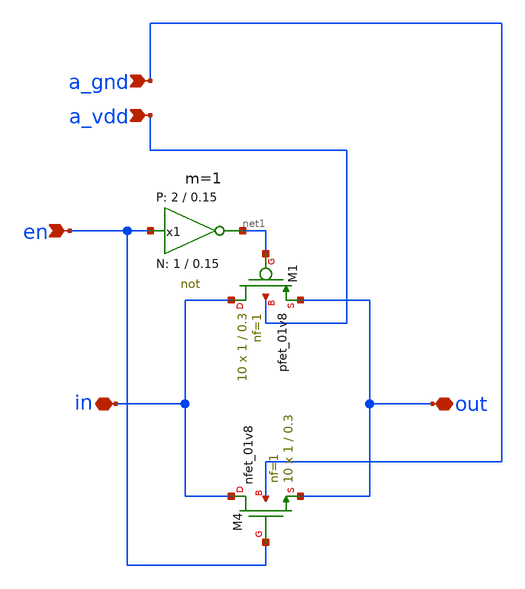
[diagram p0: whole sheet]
** sch_path: Schematics/ADC/sw/sw.sch
* StefanSchippers/xschem_sky130/sky130_tests/not.sch:
* Copyright 2021 Stefan Frederik Schippers
* Licensed under the Apache License, Version 2.0 (the "License");
**.subckt sw out in en a_gnd a_vdd
*.iopin out
*.iopin in
*.ipin en
*.ipin a_gnd
*.ipin a_vdd
XM4 in en out a_gnd sky130_fd_pr__nfet_01v8 L=0.3 W=1 nf=1 ad='int((nf+1)/2) * W/nf * 0.29' as='int((nf+2)/2) * W/nf * 0.29'
+ pd='2*int((nf+1)/2) * (W/nf + 0.29)' ps='2*int((nf+2)/2) * (W/nf + 0.29)' nrd='0.29 / W' nrs='0.29 / W'
+ sa=0 sb=0 sd=0 mult=10 m=10
XM1 in net1 out a_vdd sky130_fd_pr__pfet_01v8 L=0.3 W=1 nf=1 ad='int((nf+1)/2) * W/nf * 0.29' as='int((nf+2)/2) * W/nf * 0.29'
+ pd='2*int((nf+1)/2) * (W/nf + 0.29)' ps='2*int((nf+2)/2) * (W/nf + 0.29)' nrd='0.29 / W' nrs='0.29 / W'
+ sa=0 sb=0 sd=0 mult=10 m=10
x1 net1 en a_vdd a_gnd not W_N=1 L_N=0.15 W_P=2 L_P=0.15 m=1
**.ends

* expanding   symbol:  /home/richmond/pdk/sky130A/libs.tech/xschem/sky130_tests/not.sym # of pins=2
** sym_path: /home/richmond/pdk/sky130A/libs.tech/xschem/sky130_tests/not.sym
** sch_path: /home/richmond/pdk/sky130A/libs.tech/xschem/sky130_tests/not.sch
.subckt not y a VCCPIN VSSPIN     W_N=1 L_N=0.15 W_P=2 L_P=0.15
*.opin y
*.ipin a
XM1 DN a VSSPIN VSSPIN sky130_fd_pr__nfet_01v8 L=L_N W=W_N nf=1 ad='int((1 + 1)/2) * W_N / 1 * 0.29'
+ as='int((1 + 2)/2) * W_N / 1 * 0.29' pd='2*int((1 + 1)/2) * (W_N / 1 + 0.29)' ps='2*int((1 + 2)/2) * (W_N / 1 + 0.29)'
+ nrd='0.29 / W_N ' nrs='0.29 / W_N ' sa=0 sb=0 sd=0 mult=1 m=1
XM2 DP a VCCPIN VCCPIN sky130_fd_pr__pfet_01v8 L=L_P W=W_P nf=1 ad='int((nf+1)/2) * W/nf * 0.29' as='int((nf+2)/2) * W/nf * 0.29'
+ pd='2*int((nf+1)/2) * (W/nf + 0.29)' ps='2*int((nf+2)/2) * (W/nf + 0.29)' nrd='0.29 / W' nrs='0.29 / W'
+ sa=0 sb=0 sd=0 mult=1 m=1
Vmeas DP y 0
.save i(vmeas)
Vmeas1 y DN 0
.save i(vmeas1)
.save v(dp)
.save v(dn)
.ends

.end
